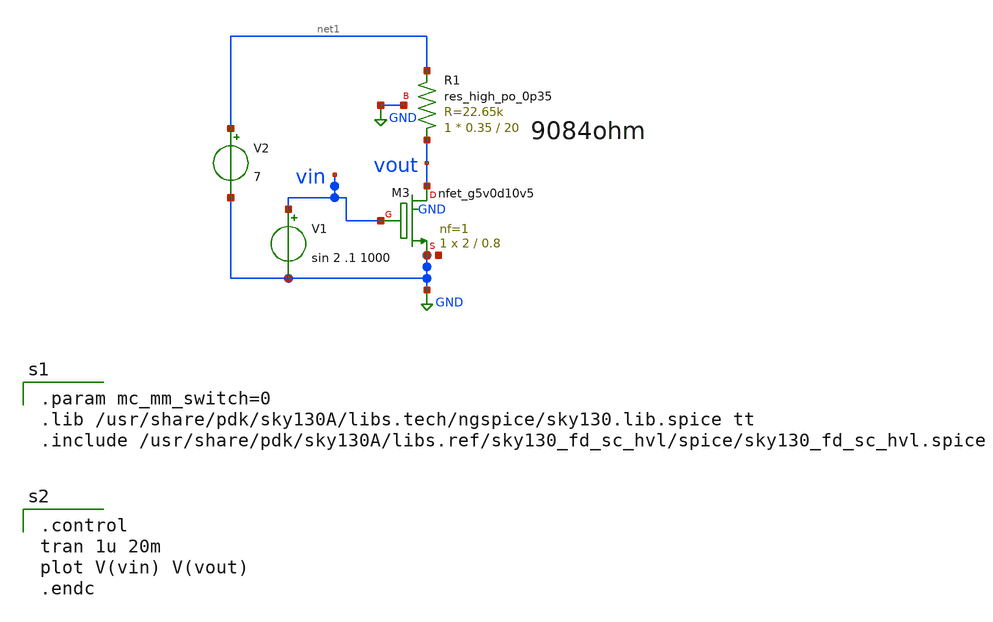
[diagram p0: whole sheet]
** sch_path: xschem/cellA.sch
**.subckt cellA
XM3 vout vin GND GND sky130_fd_pr__nfet_g5v0d10v5 L=0.8 W=2 nf=1 ad='int((nf+1)/2) * W/nf * 0.29' as='int((nf+2)/2) * W/nf * 0.29'
+ pd='2*int((nf+1)/2) * (W/nf + 0.29)' ps='2*int((nf+2)/2) * (W/nf + 0.29)' nrd='0.29 / W' nrs='0.29 / W'
+ sa=0 sb=0 sd=0 mult=1 m=1
V1 vin GND sin 2 .1 1000
XR1 vout net1 GND sky130_fd_pr__res_high_po_0p35 L=20 mult=1 m=1
V2 net1 GND 7
**** begin user architecture code

.param mc_mm_switch=0
.lib /usr/share/pdk/sky130A/libs.tech/ngspice/sky130.lib.spice tt
.include /usr/share/pdk/sky130A/libs.ref/sky130_fd_sc_hvl/spice/sky130_fd_sc_hvl.spice


.control
tran 1u 20m
plot V(vin) V(vout)
.endc

**** end user architecture code
**.ends
.GLOBAL GND
.end
